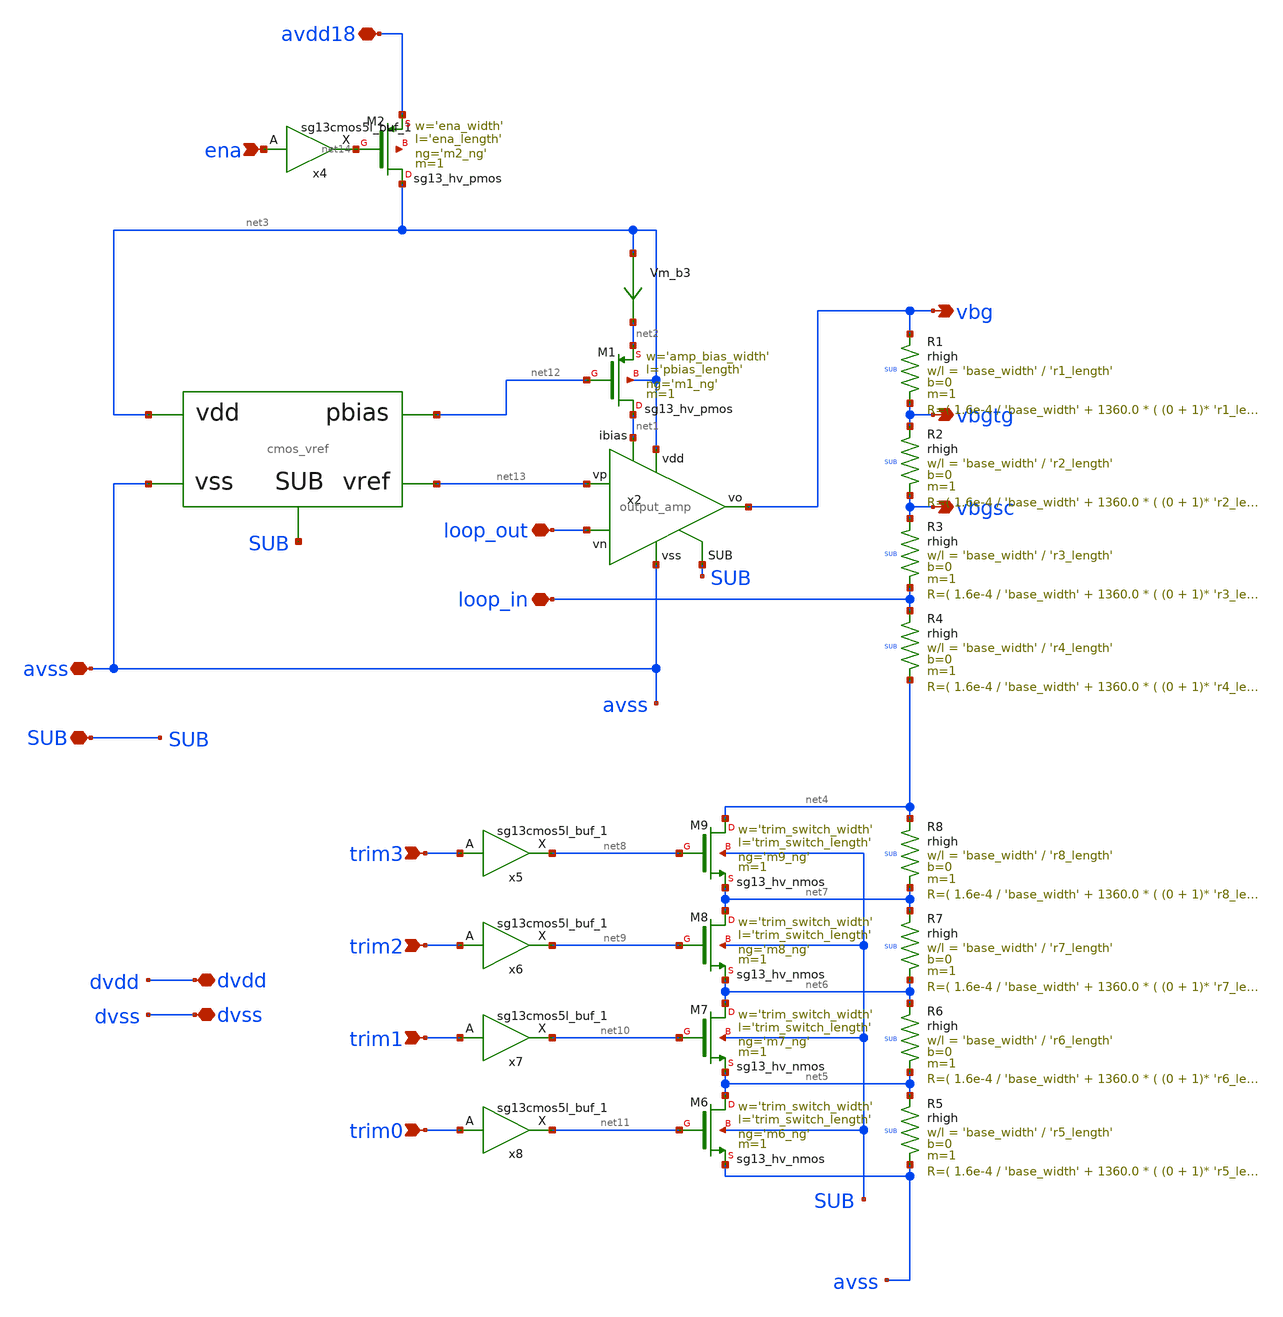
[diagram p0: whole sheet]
** sch_path: sch/top/top_default.sch
**.subckt top_default vbg avss SUB loop_in loop_out dvdd dvss vbgsc vbgtg trim3 trim2 trim1 trim0
*+ avdd18 ena
*.opin vbg
*.iopin avss
*.iopin SUB
*.iopin loop_in
*.iopin loop_out
*.iopin dvdd
*.iopin dvss
*.opin vbgsc
*.opin vbgtg
*.ipin trim3
*.ipin trim2
*.ipin trim1
*.ipin trim0
*.iopin avdd18
*.ipin ena
x2 net3 vbg net13 loop_out net1 avss SUB output_amp
Vm_b3 net3 net2 0
.save i(vm_b3)
XM1 net1 net12 net2 net3 sg13_hv_pmos w='amp_bias_width' l='pbias_length' ng='m1_ng' m=1 mm_ok=1
x5 net8 trim3 dvdd dvss sg13cmos5l_buf_1
x6 net9 trim2 dvdd dvss sg13cmos5l_buf_1
x7 net10 trim1 dvdd dvss sg13cmos5l_buf_1
x8 net11 trim0 dvdd dvss sg13cmos5l_buf_1
XR1 vbg vbgtg SUB rhigh w='base_width' l='r1_length' m=1 b=0 mm_ok=1
XR2 vbgtg vbgsc SUB rhigh w='base_width' l='r2_length' m=1 b=0 mm_ok=1
XR3 vbgsc loop_in SUB rhigh w='base_width' l='r3_length' m=1 b=0 mm_ok=1
XR4 loop_in net4 SUB rhigh w='base_width' l='r4_length' m=1 b=0 mm_ok=1
XM6 net5 net11 avss SUB sg13_hv_nmos w='trim_switch_width' l='trim_switch_length' ng='m6_ng' m=1 mm_ok=1
XM7 net6 net10 net5 SUB sg13_hv_nmos w='trim_switch_width' l='trim_switch_length' ng='m7_ng' m=1 mm_ok=1
XM8 net7 net9 net6 SUB sg13_hv_nmos w='trim_switch_width' l='trim_switch_length' ng='m8_ng' m=1 mm_ok=1
XM9 net4 net8 net7 SUB sg13_hv_nmos w='trim_switch_width' l='trim_switch_length' ng='m9_ng' m=1 mm_ok=1
XR5 net5 avss SUB rhigh w='base_width' l='r5_length' m=1 b=0 mm_ok=1
XR6 net6 net5 SUB rhigh w='base_width' l='r6_length' m=1 b=0 mm_ok=1
XR7 net7 net6 SUB rhigh w='base_width' l='r7_length' m=1 b=0 mm_ok=1
XR8 net4 net7 SUB rhigh w='base_width' l='r8_length' m=1 b=0 mm_ok=1
X1 net13 net3 avss net12 SUB cmos_vref
x4 net14 ena dvdd dvss sg13cmos5l_buf_1
XM2 net3 net14 avdd18 net15 sg13_hv_pmos w='ena_width' l='ena_length' ng='m2_ng' m=1 mm_ok=1
**.ends
.end
